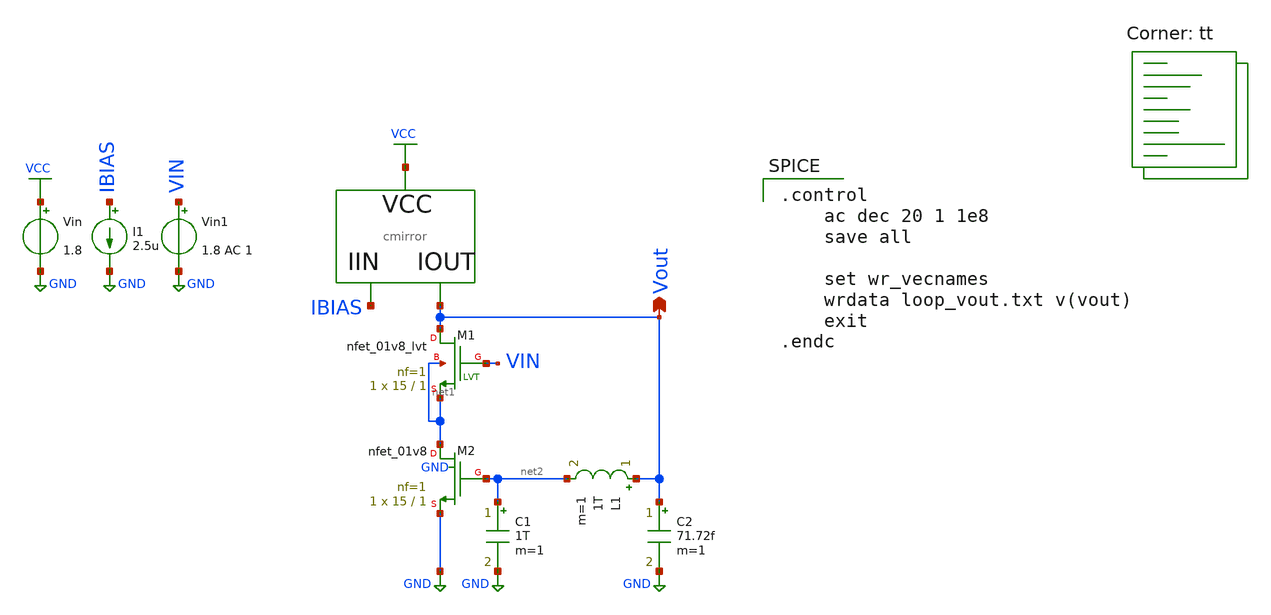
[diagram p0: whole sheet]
** sch_path: xschem/fvf_tb_loop.sch
**.subckt fvf_tb_loop Vout
*.opin Vout
Vin VCC GND 1.8
Vin1 VIN GND 1.8 AC 1
I1 IBIAS GND 2.5u
XM2 net1 net2 GND GND sky130_fd_pr__nfet_01v8 L=1 W=15 nf=1 ad='int((nf+1)/2) * W/nf * 0.29' as='int((nf+2)/2) * W/nf * 0.29'
+ pd='2*int((nf+1)/2) * (W/nf + 0.29)' ps='2*int((nf+2)/2) * (W/nf + 0.29)' nrd='0.29 / W' nrs='0.29 / W'
+ sa=0 sb=0 sd=0 mult=1 m=1
L1 Vout net2 1T m=1
C1 net2 GND 1T m=1
C2 Vout GND 71.72f m=1
cm1 VCC IBIAS Vout cmirror
XM1 Vout VIN net1 net1 sky130_fd_pr__nfet_01v8_lvt L=1 W=15 nf=1 ad='int((nf+1)/2) * W/nf * 0.29' as='int((nf+2)/2) * W/nf * 0.29'
+ pd='2*int((nf+1)/2) * (W/nf + 0.29)' ps='2*int((nf+2)/2) * (W/nf + 0.29)' nrd='0.29 / W' nrs='0.29 / W'
+ sa=0 sb=0 sd=0 mult=1 m=1
**** begin user architecture code
.lib $::SKYWATER_MODELS/sky130.lib.spice tt

.control
    ac dec 20 1 1e8
    save all

    set wr_vecnames
    wrdata loop_vout.txt v(vout)
    exit
.endc

**** end user architecture code
**.ends

* expanding   symbol:  /foss/designs/fvf-chipathon-2024/xschem/cmirror.sym # of pins=3
** sym_path: xschem/cmirror.sym
** sch_path: xschem/cmirror.sch
.subckt cmirror VCC IIN IOUT
*.ipin IIN
*.iopin VCC
*.opin IOUT
XM1 IIN IIN VCC VCC sky130_fd_pr__pfet_01v8_lvt L=1 W=2 nf=1 ad='int((nf+1)/2) * W/nf * 0.29' as='int((nf+2)/2) * W/nf * 0.29'
+ pd='2*int((nf+1)/2) * (W/nf + 0.29)' ps='2*int((nf+2)/2) * (W/nf + 0.29)' nrd='0.29 / W' nrs='0.29 / W'
+ sa=0 sb=0 sd=0 mult=2 m=2
XM2 IOUT IIN VCC VCC sky130_fd_pr__pfet_01v8_lvt L=1 W=2 nf=1 ad='int((nf+1)/2) * W/nf * 0.29' as='int((nf+2)/2) * W/nf * 0.29'
+ pd='2*int((nf+1)/2) * (W/nf + 0.29)' ps='2*int((nf+2)/2) * (W/nf + 0.29)' nrd='0.29 / W' nrs='0.29 / W'
+ sa=0 sb=0 sd=0 mult=2 m=2
.ends

.GLOBAL VCC
.GLOBAL GND
.end
